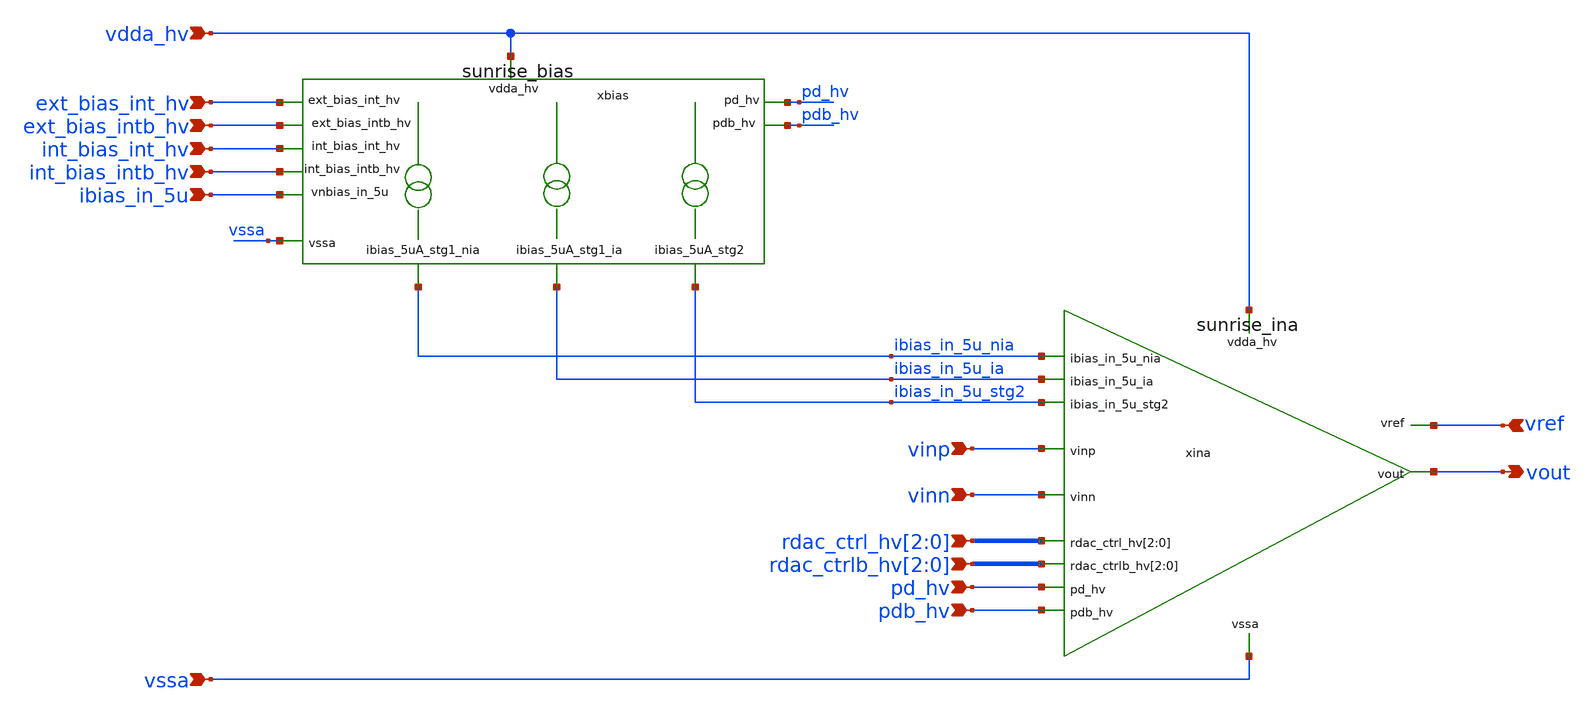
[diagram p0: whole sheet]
** sch_path: Schematics_Layout/sunrise_INA_wbias/sunrise_INA_wbias.sch
**.subckt sunrise_INA_wbias rdac_ctrl_hv[2],rdac_ctrl_hv[1],rdac_ctrl_hv[0]
*+ rdac_ctrlb_hv[2],rdac_ctrlb_hv[1],rdac_ctrlb_hv[0] pd_hv pdb_hv vinp vinn vdda_hv vref vout ext_bias_int_hv ext_bias_intb_hv int_bias_int_hv
*+ int_bias_intb_hv ibias_in_5u vssa
*.ipin rdac_ctrl_hv[2],rdac_ctrl_hv[1],rdac_ctrl_hv[0]
*.ipin rdac_ctrlb_hv[2],rdac_ctrlb_hv[1],rdac_ctrlb_hv[0]
*.ipin pd_hv
*.ipin pdb_hv
*.ipin vinp
*.ipin vinn
*.ipin vdda_hv
*.ipin vref
*.opin vout
*.ipin ext_bias_int_hv
*.ipin ext_bias_intb_hv
*.ipin int_bias_int_hv
*.ipin int_bias_intb_hv
*.ipin ibias_in_5u
*.ipin vssa
xbias vdda_hv ibias_in_5u ibias_in_5u_stg2 ibias_in_5u_ia ibias_in_5u_nia vssa int_bias_int_hv
+ int_bias_intb_hv ext_bias_int_hv ext_bias_intb_hv pd_hv pdb_hv sunrise_bias
xina vdda_hv ibias_in_5u_nia vinp pd_hv pdb_hv ibias_in_5u_stg2 vref vout rdac_ctrl_hv[2]
+ rdac_ctrl_hv[1] rdac_ctrl_hv[0] rdac_ctrlb_hv[2] rdac_ctrlb_hv[1] rdac_ctrlb_hv[0] ibias_in_5u_ia vinn vssa
+ sunrise_ina
**.ends
.end
